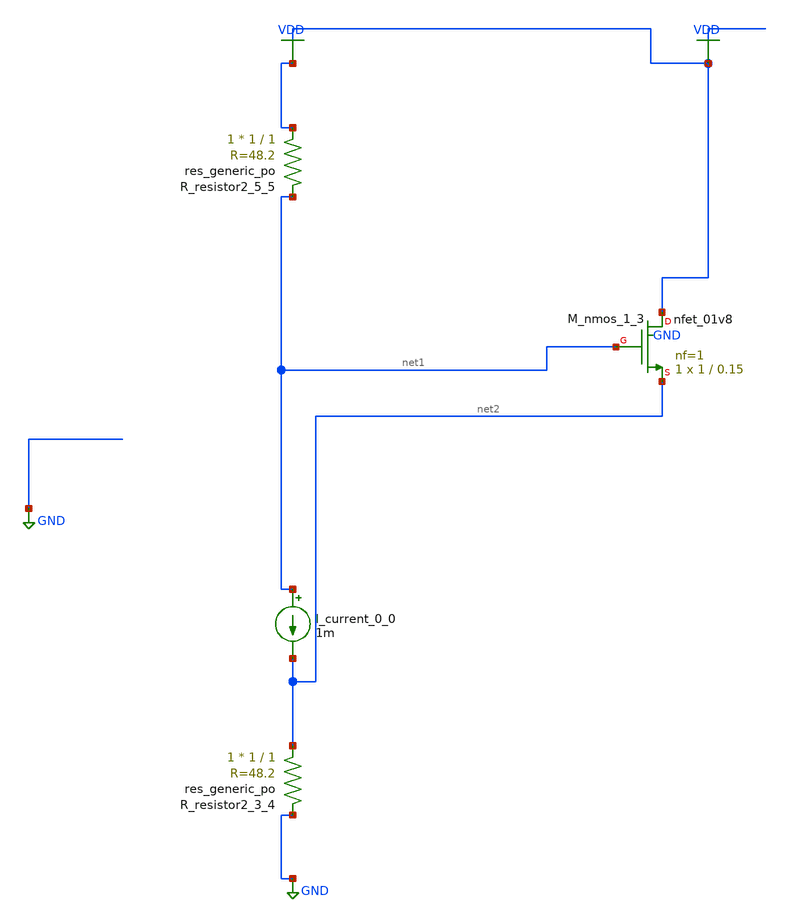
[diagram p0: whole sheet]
** sch_path: schematics/AMSNet/593.sch
**.subckt 593
I_current_0_0 net1 net2 1m
XM_nmos_1_3 VDD net1 net2 GND sky130_fd_pr__nfet_01v8 L=0.15 W=1 nf=1 ad='int((1 + 1)/2) * 1 / 1 * 0.29'
+ as='int((1 + 2)/2) * 1 / 1 * 0.29' pd='2*int((1 + 1)/2) * (1 / 1 + 0.29)' ps='2*int((1 + 2)/2) * (1 / 1 + 0.29)'
+ nrd='0.29 / 1 ' nrs='0.29 / 1 ' sa=0 sb=0 sd=0 mult=1 m=1
XR_resistor2_3_4 net2 GND sky130_fd_pr__res_generic_po W=1 L=1 m=1
XR_resistor2_5_5 VDD net1 sky130_fd_pr__res_generic_po W=1 L=1 m=1
**.ends
.GLOBAL GND
.GLOBAL VDD
.end
